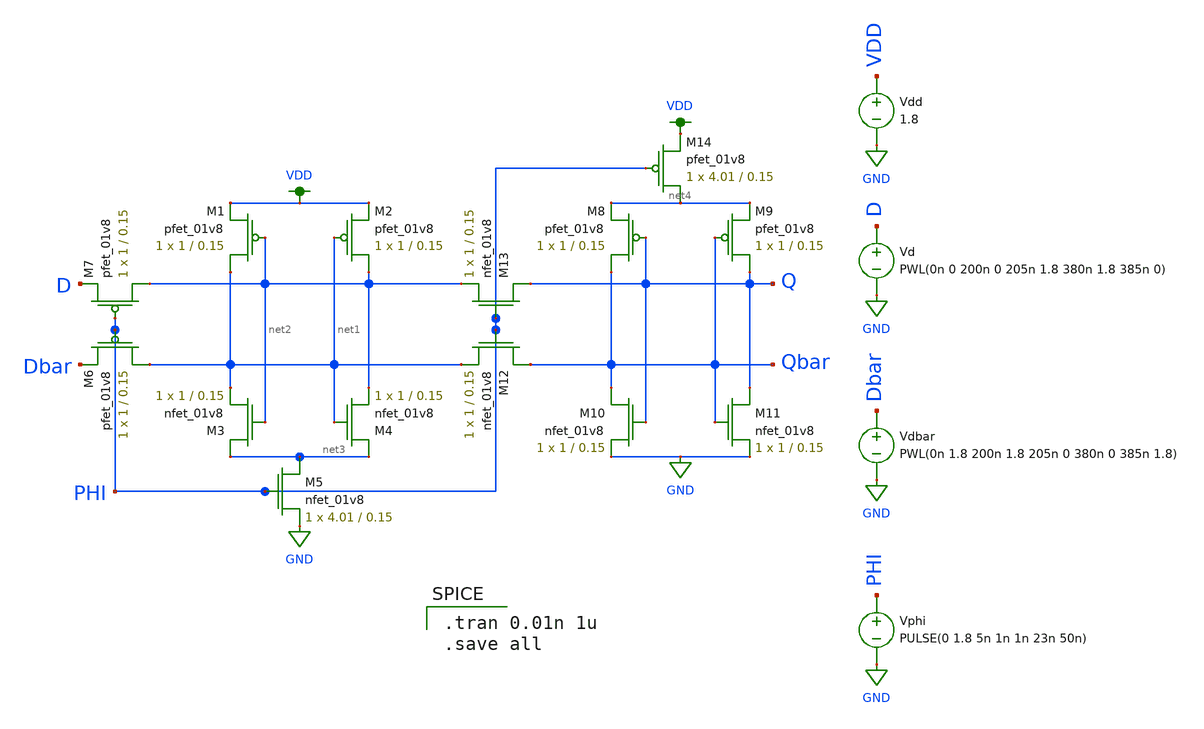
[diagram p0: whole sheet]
** sch_path: mp2/latch_testharness.sch
**.subckt latch_testharness
XM1 net1 net2 VDD VDD sky130_fd_pr__pfet_01v8 L=0.15 W=1 nf=1 ad='int((nf+1)/2) * W/nf * 0.29' as='int((nf+2)/2) * W/nf * 0.29'
+ pd='2*int((nf+1)/2) * (W/nf + 0.29)' ps='2*int((nf+2)/2) * (W/nf + 0.29)' nrd='0.29 / W' nrs='0.29 / W'
+ sa=0 sb=0 sd=0 mult=1 m=1
XM2 net2 net1 VDD VDD sky130_fd_pr__pfet_01v8 L=0.15 W=1 nf=1 ad='int((nf+1)/2) * W/nf * 0.29' as='int((nf+2)/2) * W/nf * 0.29'
+ pd='2*int((nf+1)/2) * (W/nf + 0.29)' ps='2*int((nf+2)/2) * (W/nf + 0.29)' nrd='0.29 / W' nrs='0.29 / W'
+ sa=0 sb=0 sd=0 mult=1 m=1
XM3 net3 net2 net1 GND sky130_fd_pr__nfet_01v8 L=0.15 W=1 nf=1 ad='int((nf+1)/2) * W/nf * 0.29' as='int((nf+2)/2) * W/nf * 0.29'
+ pd='2*int((nf+1)/2) * (W/nf + 0.29)' ps='2*int((nf+2)/2) * (W/nf + 0.29)' nrd='0.29 / W' nrs='0.29 / W'
+ sa=0 sb=0 sd=0 mult=1 m=1
XM4 net3 net1 net2 GND sky130_fd_pr__nfet_01v8 L=0.15 W=1 nf=1 ad='int((nf+1)/2) * W/nf * 0.29' as='int((nf+2)/2) * W/nf * 0.29'
+ pd='2*int((nf+1)/2) * (W/nf + 0.29)' ps='2*int((nf+2)/2) * (W/nf + 0.29)' nrd='0.29 / W' nrs='0.29 / W'
+ sa=0 sb=0 sd=0 mult=1 m=1
XM5 net3 PHI GND GND sky130_fd_pr__nfet_01v8 L=0.15 W=4.01 nf=1 ad='int((nf+1)/2) * W/nf * 0.29' as='int((nf+2)/2) * W/nf * 0.29'
+ pd='2*int((nf+1)/2) * (W/nf + 0.29)' ps='2*int((nf+2)/2) * (W/nf + 0.29)' nrd='0.29 / W' nrs='0.29 / W'
+ sa=0 sb=0 sd=0 mult=1 m=1
XM6 net1 PHI Dbar VDD sky130_fd_pr__pfet_01v8 L=0.15 W=1 nf=1 ad='int((nf+1)/2) * W/nf * 0.29' as='int((nf+2)/2) * W/nf * 0.29'
+ pd='2*int((nf+1)/2) * (W/nf + 0.29)' ps='2*int((nf+2)/2) * (W/nf + 0.29)' nrd='0.29 / W' nrs='0.29 / W'
+ sa=0 sb=0 sd=0 mult=1 m=1
XM7 net2 PHI D VDD sky130_fd_pr__pfet_01v8 L=0.15 W=1 nf=1 ad='int((nf+1)/2) * W/nf * 0.29' as='int((nf+2)/2) * W/nf * 0.29'
+ pd='2*int((nf+1)/2) * (W/nf + 0.29)' ps='2*int((nf+2)/2) * (W/nf + 0.29)' nrd='0.29 / W' nrs='0.29 / W'
+ sa=0 sb=0 sd=0 mult=1 m=1
XM8 Qbar Q net4 VDD sky130_fd_pr__pfet_01v8 L=0.15 W=1 nf=1 ad='int((nf+1)/2) * W/nf * 0.29' as='int((nf+2)/2) * W/nf * 0.29'
+ pd='2*int((nf+1)/2) * (W/nf + 0.29)' ps='2*int((nf+2)/2) * (W/nf + 0.29)' nrd='0.29 / W' nrs='0.29 / W'
+ sa=0 sb=0 sd=0 mult=1 m=1
XM9 Q Qbar net4 VDD sky130_fd_pr__pfet_01v8 L=0.15 W=1 nf=1 ad='int((nf+1)/2) * W/nf * 0.29' as='int((nf+2)/2) * W/nf * 0.29'
+ pd='2*int((nf+1)/2) * (W/nf + 0.29)' ps='2*int((nf+2)/2) * (W/nf + 0.29)' nrd='0.29 / W' nrs='0.29 / W'
+ sa=0 sb=0 sd=0 mult=1 m=1
XM10 Qbar Q GND GND sky130_fd_pr__nfet_01v8 L=0.15 W=1 nf=1 ad='int((nf+1)/2) * W/nf * 0.29' as='int((nf+2)/2) * W/nf * 0.29'
+ pd='2*int((nf+1)/2) * (W/nf + 0.29)' ps='2*int((nf+2)/2) * (W/nf + 0.29)' nrd='0.29 / W' nrs='0.29 / W'
+ sa=0 sb=0 sd=0 mult=1 m=1
XM11 Q Qbar GND GND sky130_fd_pr__nfet_01v8 L=0.15 W=1 nf=1 ad='int((nf+1)/2) * W/nf * 0.29' as='int((nf+2)/2) * W/nf * 0.29'
+ pd='2*int((nf+1)/2) * (W/nf + 0.29)' ps='2*int((nf+2)/2) * (W/nf + 0.29)' nrd='0.29 / W' nrs='0.29 / W'
+ sa=0 sb=0 sd=0 mult=1 m=1
XM12 Qbar PHI net1 GND sky130_fd_pr__nfet_01v8 L=0.15 W=1 nf=1 ad='int((nf+1)/2) * W/nf * 0.29' as='int((nf+2)/2) * W/nf * 0.29'
+ pd='2*int((nf+1)/2) * (W/nf + 0.29)' ps='2*int((nf+2)/2) * (W/nf + 0.29)' nrd='0.29 / W' nrs='0.29 / W'
+ sa=0 sb=0 sd=0 mult=1 m=1
XM13 Q PHI net2 GND sky130_fd_pr__nfet_01v8 L=0.15 W=1 nf=1 ad='int((nf+1)/2) * W/nf * 0.29' as='int((nf+2)/2) * W/nf * 0.29'
+ pd='2*int((nf+1)/2) * (W/nf + 0.29)' ps='2*int((nf+2)/2) * (W/nf + 0.29)' nrd='0.29 / W' nrs='0.29 / W'
+ sa=0 sb=0 sd=0 mult=1 m=1
XM14 net4 PHI VDD VDD sky130_fd_pr__pfet_01v8 L=0.15 W=4.01 nf=1 ad='int((nf+1)/2) * W/nf * 0.29' as='int((nf+2)/2) * W/nf * 0.29'
+ pd='2*int((nf+1)/2) * (W/nf + 0.29)' ps='2*int((nf+2)/2) * (W/nf + 0.29)' nrd='0.29 / W' nrs='0.29 / W'
+ sa=0 sb=0 sd=0 mult=1 m=1
Vd D GND PWL(0n 0 200n 0 205n 1.8 380n 1.8 385n 0)
Vdbar Dbar GND PWL(0n 1.8 200n 1.8 205n 0 380n 0 385n 1.8)
Vphi PHI GND PULSE(0 1.8 5n 1n 1n 23n 50n)
Vdd VDD GND 1.8
**** begin user architecture code

.tran 0.01n 1u
.save all


.option wnflag=1
.lib ~/skywater/skywater-pdk/libraries/sky130_fd_pr_ngspice/latest/models/sky130.lib.spice ff

**** end user architecture code
**.ends
.GLOBAL GND
.GLOBAL VDD
.end
